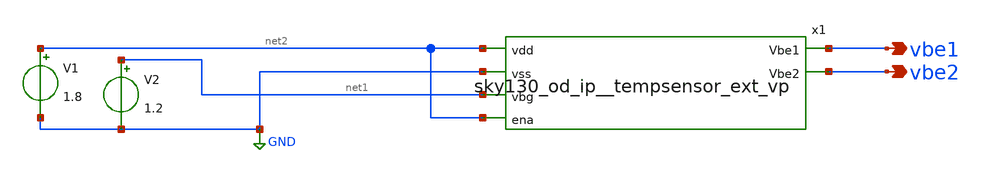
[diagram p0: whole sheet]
** sch_path: xschem/sky130_od_ip__tempsensor_ex_vp_tb.sch
**.subckt sky130_od_ip__tempsensor_ex_vp_tb vbe1 vbe2
*.opin vbe1
*.opin vbe2
V1 net2 GND 1.8
x1 net2 GND net1 vbe1 vbe2 net2 sky130_od_ip__tempsensor_ext_vp
V2 net1 GND 1.2
**** begin user architecture code

.lib /usr/local/share/pdk/sky130A/libs.tech/ngspice/sky130.lib.spice tt



.func mu(vbe1,vbe2) = 10.7906/(10.7906+vbe1/(vbe2-vbe1))
.func T(mu) = 714.015*mu-259.802
.control
option TEMP=25
op
let ttrim = T(mu(V(vbe1),V(vbe2)))-25
*let ttrim=0
*print ttrim
*** DEBUG - search for linear mode trasistor
set altshow
show > /tmp/tras.txt

dc temp -40 125 10
plot V(vbe1) V(vbe2)-V(vbe1) V(vbe1)+10.7906*(V(vbe2)-V(vbe1))
plot T(mu(V(vbe1),V(vbe2)))-op1.ttrim
plot T(mu(V(vbe1),V(vbe2)))-"temp-sweep"-op1.ttrim
plot V(vbe1) V(vbe2)


.endc

**** end user architecture code
**.ends

* expanding   symbol:  xschem/sky130_od_ip__tempsensor_ext_vp.sym # of pins=6
** sym_path: xschem/sky130_od_ip__tempsensor_ext_vp.sym
** sch_path: xschem/sky130_od_ip__tempsensor_ext_vp.sch
.subckt sky130_od_ip__tempsensor_ext_vp vdd vss vbg Vbe1 Vbe2 ena
*.ipin vdd
*.ipin vss
*.opin Vbe2
*.opin Vbe1
*.ipin ena
*.ipin vbg
XQ_BL1 vss vss Vbe1 sky130_fd_pr__pnp_05v5_W3p40L3p40 m=1
XQ_BR1 vss vss Vbe2 sky130_fd_pr__pnp_05v5_W3p40L3p40 m=1
XM1 Vbe1 vp vdd VDD sky130_fd_pr__pfet_01v8_lvt L=1 W=1 nf=1 ad='int((nf+1)/2) * W/nf * 0.29' as='int((nf+2)/2) * W/nf * 0.29'
+ pd='2*int((nf+1)/2) * (W/nf + 0.29)' ps='2*int((nf+2)/2) * (W/nf + 0.29)' nrd='0.29 / W' nrs='0.29 / W'
+ sa=0 sb=0 sd=0 mult=1 m=1
XM2 Vbe2 vp vdd VDD sky130_fd_pr__pfet_01v8_lvt L=1 W=1 nf=1 ad='int((nf+1)/2) * W/nf * 0.29' as='int((nf+2)/2) * W/nf * 0.29'
+ pd='2*int((nf+1)/2) * (W/nf + 0.29)' ps='2*int((nf+2)/2) * (W/nf + 0.29)' nrd='0.29 / W' nrs='0.29 / W'
+ sa=0 sb=0 sd=0 mult=5 m=5
XM4 net2 vbg net1 vss sky130_fd_pr__nfet_01v8 L=1 W=1 nf=1 ad='int((nf+1)/2) * W/nf * 0.29' as='int((nf+2)/2) * W/nf * 0.29'
+ pd='2*int((nf+1)/2) * (W/nf + 0.29)' ps='2*int((nf+2)/2) * (W/nf + 0.29)' nrd='0.29 / W' nrs='0.29 / W'
+ sa=0 sb=0 sd=0 mult=1 m=1
XM5 vp vp net1 vss sky130_fd_pr__nfet_01v8 L=1 W=1 nf=1 ad='int((nf+1)/2) * W/nf * 0.29' as='int((nf+2)/2) * W/nf * 0.29'
+ pd='2*int((nf+1)/2) * (W/nf + 0.29)' ps='2*int((nf+2)/2) * (W/nf + 0.29)' nrd='0.29 / W' nrs='0.29 / W'
+ sa=0 sb=0 sd=0 mult=1 m=1
XM7 vp net2 vdd vdd sky130_fd_pr__pfet_01v8 L=1 W=10 nf=1 ad='int((nf+1)/2) * W/nf * 0.29' as='int((nf+2)/2) * W/nf * 0.29'
+ pd='2*int((nf+1)/2) * (W/nf + 0.29)' ps='2*int((nf+2)/2) * (W/nf + 0.29)' nrd='0.29 / W' nrs='0.29 / W'
+ sa=0 sb=0 sd=0 mult=1 m=1
XM8 net2 net2 vdd vdd sky130_fd_pr__pfet_01v8 L=1 W=10 nf=1 ad='int((nf+1)/2) * W/nf * 0.29' as='int((nf+2)/2) * W/nf * 0.29'
+ pd='2*int((nf+1)/2) * (W/nf + 0.29)' ps='2*int((nf+2)/2) * (W/nf + 0.29)' nrd='0.29 / W' nrs='0.29 / W'
+ sa=0 sb=0 sd=0 mult=1 m=1
XM3 vp ena vdd vdd sky130_fd_pr__pfet_01v8 L=1 W=1 nf=1 ad='int((nf+1)/2) * W/nf * 0.29' as='int((nf+2)/2) * W/nf * 0.29'
+ pd='2*int((nf+1)/2) * (W/nf + 0.29)' ps='2*int((nf+2)/2) * (W/nf + 0.29)' nrd='0.29 / W' nrs='0.29 / W'
+ sa=0 sb=0 sd=0 mult=1 m=1
XM6 net1 ena vss vss sky130_fd_pr__nfet_01v8 L=20 W=1 nf=1 ad='int((nf+1)/2) * W/nf * 0.29' as='int((nf+2)/2) * W/nf * 0.29'
+ pd='2*int((nf+1)/2) * (W/nf + 0.29)' ps='2*int((nf+2)/2) * (W/nf + 0.29)' nrd='0.29 / W' nrs='0.29 / W'
+ sa=0 sb=0 sd=0 mult=1 m=1
.ends

.GLOBAL GND
.end
